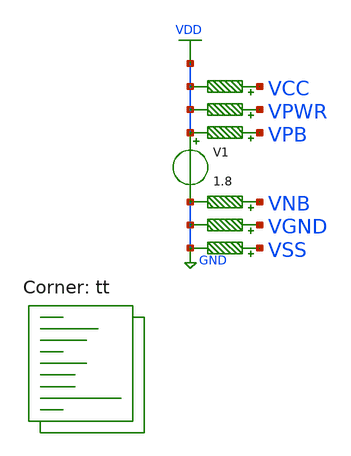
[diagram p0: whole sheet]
** sch_path: test.sch
**.subckt test
V1 VDD GND 1.8
R1 VPB VDD 0.01 m=1
R2 VPWR VDD 0.01 m=1
R3 VCC VDD 0.01 m=1
R4 VNB GND 0.01 m=1
R5 VGND GND 0.01 m=1
R6 VSS GND 0.01 m=1
**** begin user architecture code
.lib $::SKYWATER_MODELS/sky130.lib.spice tt


.include /usr/local/share/pdk/sky130A/libs.ref/sky130_fd_sc_hd/spice/sky130_fd_sc_hd.spice tt
.control
  save all
  tran 1n 10u
  write top.raw
  quit 0
.endc


**** end user architecture code
**.ends
.GLOBAL VDD
.GLOBAL GND
**** begin user architecture code


.GLOBAL VDD
.GLOBAL GND
.GLOBAL VCC
.GLOBAL VPWR
.GLOBAL VPB
.GLOBAL VNB
.GLOBAL VGND
.GLOBAL VSS


**** end user architecture code
.end
